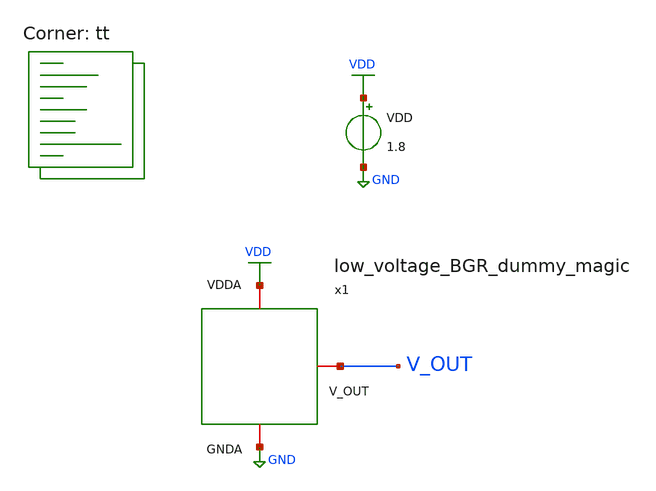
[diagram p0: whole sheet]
** sch_path: projects/bandgapref/xschem_ngspice/new_files/tb_low_voltage_BGR_dummy_magic.sch
**.subckt tb_low_voltage_BGR_dummy_magic
VDD VDD GND 1.8
x1 VDD V_OUT GND low_voltage_BGR_dummy_magic
**** begin user architecture code
.lib $::SKYWATER_MODELS/sky130.lib.spice tt



.include /foss/designs/my_design/projects/bandgapref/xschem_ngspice/new_files/low_voltage_BGR_dummy_magic.spice

.option method=gear
.option wnflag=1
* .option savecurrents
* .option gmin=5n

.save
* +@m.x1.x1.msky130_fd_pr__pfet_01v8[gm]
* +@m.x1.x9.msky130_fd_pr__pfet_01v8[gm]
* +@m.x1.x32.msky130_fd_pr__pfet_01v8[gm]

* .ic v(vin-) = 0.8
* .ic v(x1.v_top.n0) = 1.8

.control

  * let runs=10
  * let run=1

  * dowhile run <= runs

    save v(x1.v_out.n0) v(x1.vdda.n0) v(x1.v_top.n0) v(x1.vin-.n0) v(x1.vin+.n0)
    * save all
    * dc temp -40 120 1 VDD 0 2.0 0.1
    dc VDD 0 2.0 0.01 temp -40 120 20
    * dc VDD 0 2.0 0.01
    * tran 1ns 20us
    remzerovec
    write tb_low_voltage_BGR_dummy_magic.raw
    * write tb_low_voltage_BGR_dummy_magic_mc.raw
    * write tb_low_voltage_BGR_dummy_magic_tran.raw
    * write tb_low_voltage_BGR_dummy_magic_tran_mc.raw
    * write tb_low_voltage_BGR_dummy_magic_vdd_temp_tt.raw
    * write tb_low_voltage_BGR_dummy_magic_vdd_temp_fs.raw
    * write tb_low_voltage_BGR_dummy_magic_vdd_temp_sf.raw
    * write tb_low_voltage_BGR_dummy_magic_vdd_temp_ff.raw
    * write tb_low_voltage_BGR_dummy_magic_temp_vdd_tt.raw
    * write tb_low_voltage_BGR_dummy_magic_temp_vdd_sf.raw
    * write tb_low_voltage_BGR_dummy_magic_temp_vdd_fs.raw
    * write tb_low_voltage_BGR_dummy_magic_temp_vdd_ss.raw
    * write tb_low_voltage_BGR_dummy_magic_temp_vdd_ff.raw
    set appendwrite
    * reset
    * let run = run + 1
  * end
.endc



**** end user architecture code
**.ends
.GLOBAL GND
.GLOBAL VDD
.end
